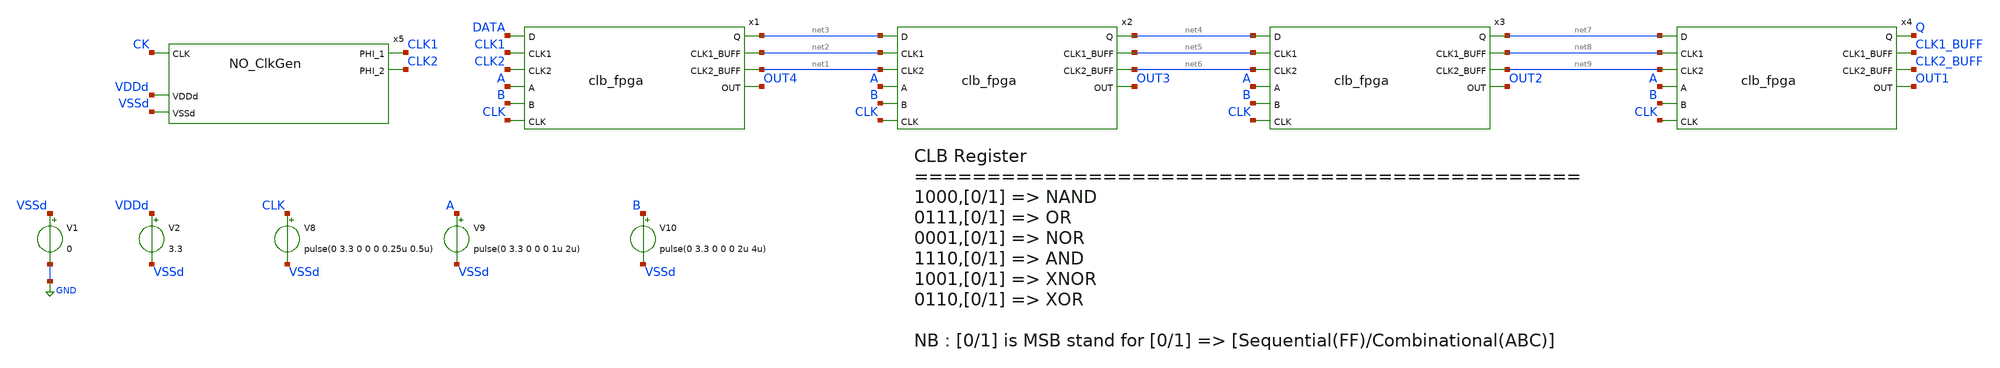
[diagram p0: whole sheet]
** sch_path: designs/libs/tb_fpga/tb_clb/tb_clb.sch
**.subckt tb_clb
x1 DATA CLK1 CLK2 A B CLK net3 net2 net1 OUT4 clb_fpga
V1 VSSd GND 0
V2 VDDd VSSd 3.3
V8 CLK VSSd pulse(0 3.3 0 0 0 0.25u 0.5u)
V9 A VSSd pulse(0 3.3 0 0 0 1u 2u)
V10 B VSSd pulse(0 3.3 0 0 0 2u 4u)
x2 net3 net2 net1 A B CLK net4 net5 net6 OUT3 clb_fpga
x3 net4 net5 net6 A B CLK net7 net8 net9 OUT2 clb_fpga
x4 net7 net8 net9 A B CLK Q CLK1_BUFF CLK2_BUFF OUT1 clb_fpga
x5 CLK2 CK CLK1 VDDd VSSd NO_ClkGen
**** begin user architecture code


.global VDDd VSSd
* clock
abit [ bit_node ]  input_vector
.model input_vector
+ d_source(input_file="/foss/designs/sscs-chipathon2025-LNA/designs/libs/tb_fpga/tb_clb/data.txt")
* data
aclock [ clock_node ] clock_vector
.model clock_vector
+ d_source(input_file="/foss/designs/sscs-chipathon2025-LNA/designs/libs/tb_fpga/tb_clb/data_clk.txt")
* convert digital signals to analog
aconvert [ bit_node clock_node ] [ data ck ] dac_in
.model dac_in dac_bridge (out_low=0V out_high=3.3V t_rise=0.2ns t_fall=0.2ns)

.control

    save all
    TRAN 0.2n 10u
    write tb_clb.raw

.endc



.include /foss/pdks/gf180mcuD/libs.ref/gf180mcu_fd_sc_mcu9t5v0/spice/gf180mcu_fd_sc_mcu9t5v0.spice
.include $::180MCU_MODELS/design.ngspice
.lib $::180MCU_MODELS/sm141064.ngspice typical

**** end user architecture code
**.ends
.GLOBAL GND
.end
